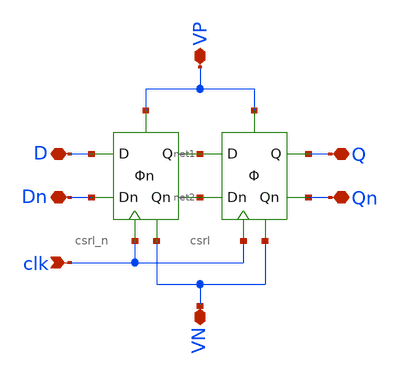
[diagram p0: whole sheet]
** sch_path: lib/digital/schematic/csrl_rising_edge.sch
**.subckt csrl_rising_edge clk D Dn Q Qn VP VN
*.ipin clk
*.iopin D
*.iopin Dn
*.iopin Q
*.iopin Qn
*.iopin VP
*.iopin VN
X1 net1 net2 Qn Q VN clk VP csrl
X2 D Dn net2 net1 VN clk VP csrl_n
**.ends
.end
